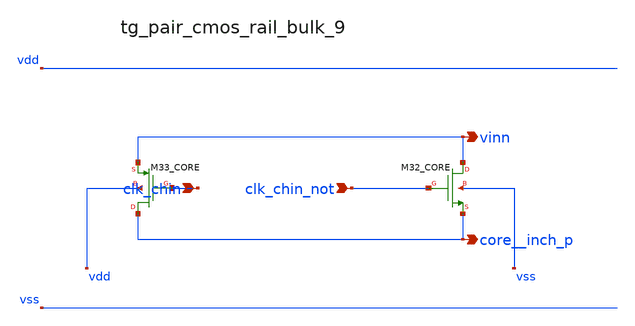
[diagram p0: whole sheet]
** sch_path: analog-db/raw/ia_006_fan_chopper_cmfb/hier/blocks/tg_pair_cmos_rail_bulk_9.sch
**.subckt tg_pair_cmos_rail_bulk_9 clk_chin clk_chin_not vinn core__inch_p
*.ipin clk_chin
*.ipin clk_chin_not
*.opin vinn
*.opin core__inch_p
XM32_CORE vinn clk_chin_not core__inch_p vss sg13_lv_nmos w=x_dut_xm32_core_w l=x_dut_xm32_core_l
+ ng=1 m=x_dut_xm32_core_m
XM33_CORE core__inch_p clk_chin vinn vdd sg13_lv_pmos w=x_dut_xm33_core_w l=x_dut_xm33_core_l ng=1
+ m=x_dut_xm33_core_m
**.ends
.end
